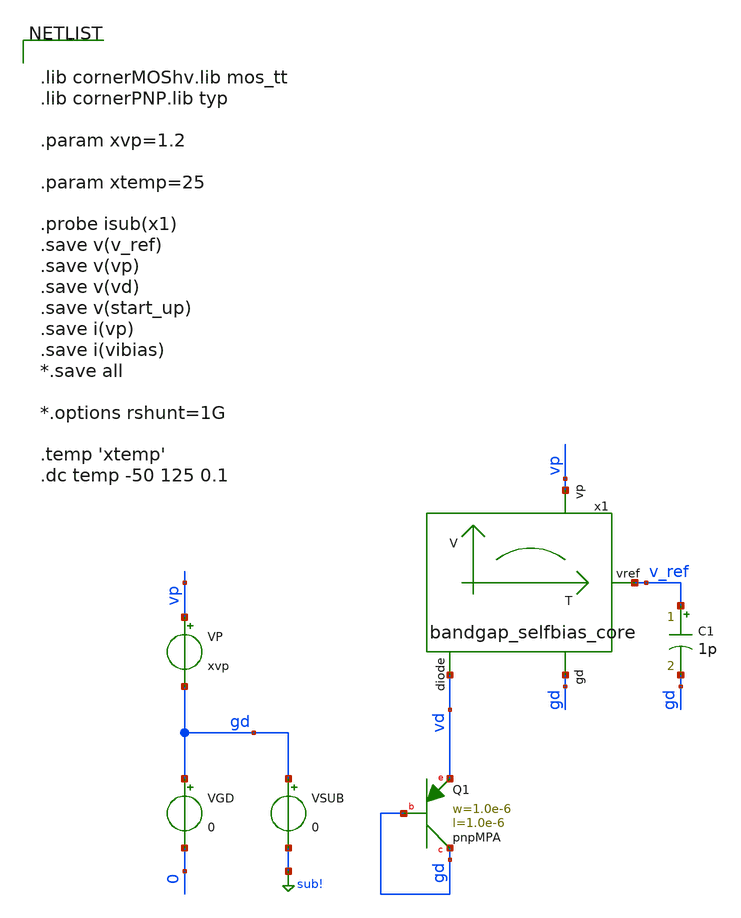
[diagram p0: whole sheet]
** sch_path: testbench/bandgap_selfbias_core_temp_sweep_tb.sch
**.subckt bandgap_selfbias_core_temp_sweep_tb
VGD gd 0 0
VP vp gd xvp
.save i(vp)
VSUB gd sub! 0
C1 v_ref gd 1p m=1
x1 vp v_ref gd vd bandgap_selfbias_core
XQ1 gd gd vd pnpMPA a=1p p=4u m=1
**** begin user architecture code


.lib cornerMOShv.lib mos_tt
.lib cornerPNP.lib typ

.param xvp=1.2

.param xtemp=25

.probe isub(x1)
.save v(v_ref)
.save v(vp)
.save v(vd)
.save v(start_up)
.save i(vp)
.save i(vibias)
*.save all

*.options rshunt=1G

.temp 'xtemp'
.dc temp -50 125 0.1


**** end user architecture code
**.ends

* expanding   symbol:  /foss/designs/test/circuit/bandgap_selfbias_core.sym # of pins=4
** sym_path: circuit/bandgap_selfbias_core.sym
** sch_path: circuit/bandgap_selfbias_core.sch
.subckt bandgap_selfbias_core vp vref gd diode
*.opin diode
*.ipin gd
*.ipin vp
*.opin vref
XM1 net1 net1 gd gd sg13_hv_nmos w=1.2u l=0.9u ng=1 m=8 mm_ok=1
XM2 net2 diode net1 gd sg13_hv_nmos w=1.2u l=0.9u ng=1 m=8 mm_ok=1
XM3 net4 diode net2 gd sg13_hv_nmos w=1.2u l=0.9u ng=1 m=24 mm_ok=1
XM4 net4 net4 vp vp sg13_hv_pmos w=1.2u l=1.8u ng=1 m=8 mm_ok=1
XM5 net5 net3 net2 gd sg13_hv_nmos w=1.2u l=0.9u ng=1 m=8 mm_ok=1
XM6 net3 net3 net5 gd sg13_hv_nmos w=1.2u l=0.9u ng=1 m=16 mm_ok=1
XM7 net3 net4 vp vp sg13_hv_pmos w=1.2u l=1.8u ng=1 m=2 mm_ok=1
XM8 vref net6 net5 gd sg13_hv_nmos w=1.2u l=0.9u ng=1 m=8 mm_ok=1
XM9 net6 net6 vref gd sg13_hv_nmos w=1.2u l=0.9u ng=1 m=16 mm_ok=1
XM10 net6 net4 vp vp sg13_hv_pmos w=1.2u l=1.8u ng=1 m=2 mm_ok=1
XM11 vref net4 vp vp sg13_hv_pmos w=1.2u l=1.8u ng=1 m=4 mm_ok=1
XM12 diode net4 vp vp sg13_hv_pmos w=1.2u l=1.8u ng=1 m=16 mm_ok=1
.ends

.GLOBAL sub!
.end
